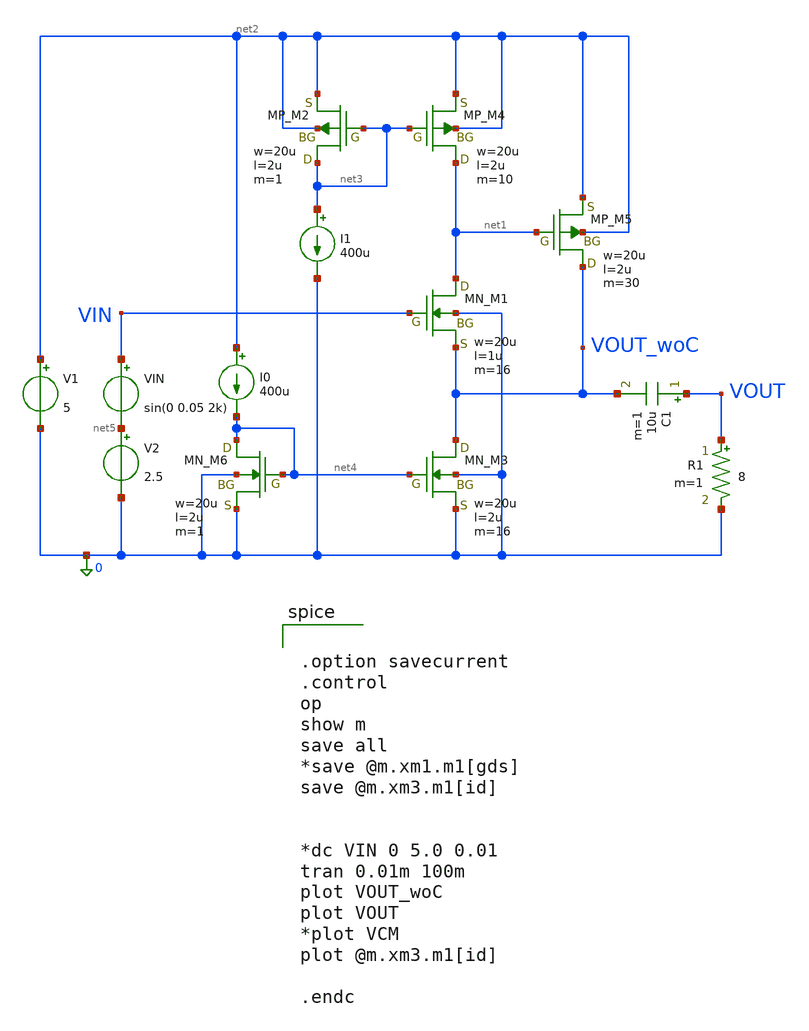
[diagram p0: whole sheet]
** sch_path: member_project/JJY_Receiver/Masahiro/jjy_recv/OBUF_SSF/SSF_sim_flat.sch
**.subckt SSF_sim_flat
V1 net2 0 5
VIN VIN net5 sin(0 0.05 2k)
R1 VOUT 0 8 m=1
V2 net5 0 2.5
C1 VOUT VOUT_woC 10u m=1
XM1 net1 VIN VOUT_woC 0 NMOS w=20u l=1u as=0 ad=0 ps=0 pd=0 nrd=0 nrs=0 m=16
XM3 VOUT_woC net4 0 0 NMOS w=20u l=2u as=0 ad=0 ps=0 pd=0 nrd=0 nrs=0 m=16
XM6 net4 net4 0 0 NMOS w=20u l=2u as=0 ad=0 ps=0 pd=0 nrd=0 nrs=0 m=1
I0 net2 net4 400u
I1 net3 0 400u
XM2 net3 net3 net2 net2 PMOS w=20u l=2u as=0 ad=0 ps=0 pd=0 nrd=0 nrs=0 m=1
XM4 net1 net3 net2 net2 PMOS w=20u l=2u as=0 ad=0 ps=0 pd=0 nrd=0 nrs=0 m=10
XM5 VOUT_woC net1 net2 net2 PMOS w=20u l=2u as=0 ad=0 ps=0 pd=0 nrd=0 nrs=0 m=30
**** begin user architecture code
 .include $::LIB/ip62_models


.option savecurrent
.control
op
show m
save all
*save @m.xm1.m1[gds]
save @m.xm3.m1[id]


*dc VIN 0 5.0 0.01
tran 0.01m 100m
plot VOUT_woC
plot VOUT
*plot VCM
plot @m.xm3.m1[id]

.endc


**** end user architecture code
**.ends
.end
